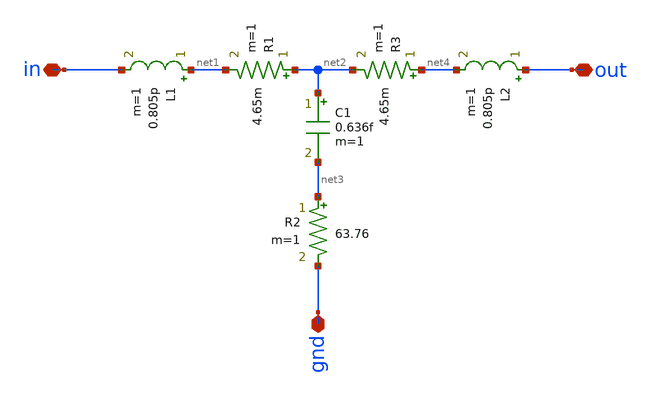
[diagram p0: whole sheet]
** sch_path: VGA_tapeout/xschem/sims/SCPWm2_segment_3um.sch
**.subckt SCPWm2_segment_3um in out gnd
*.iopin in
*.iopin out
*.iopin gnd
L1 net1 in 0.805p m=1
C1 net2 net3 0.636f m=1
R1 net2 net1 4.65m m=1
R2 net3 gnd 63.76 m=1
R3 net4 net2 4.65m m=1
L2 out net4 0.805p m=1
**.ends
.end
